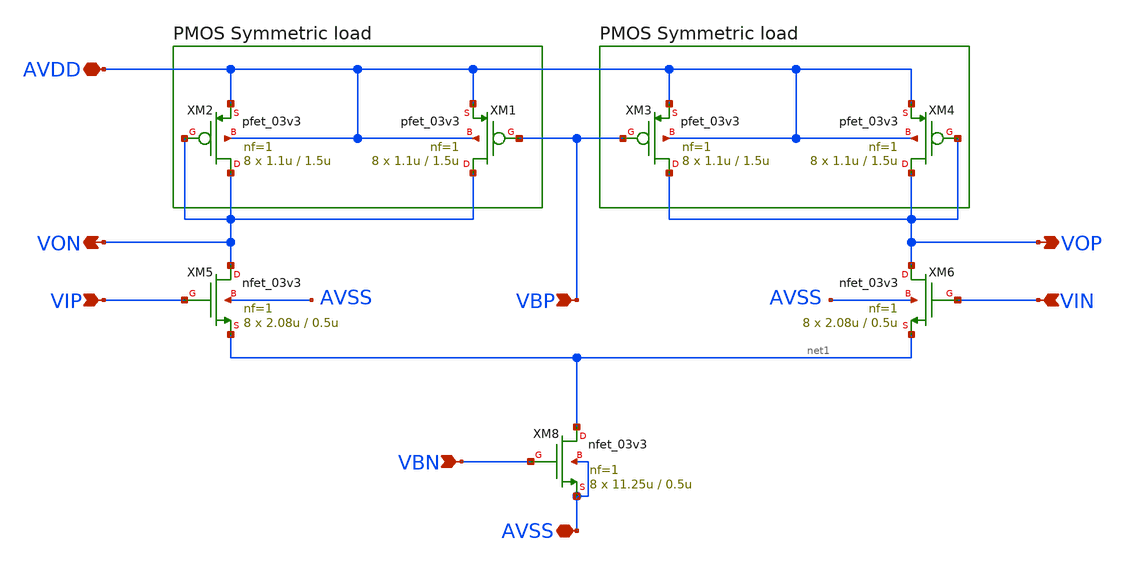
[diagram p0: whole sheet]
** sch_path: designs/libs/core_analog/delay_stage/delay_stage.sch
**.subckt delay_stage VIP VIN VOP VON AVDD AVSS VBP VBN
*.ipin VIP
*.ipin VIN
*.opin VOP
*.opin VON
*.iopin AVDD
*.iopin AVSS
*.ipin VBP
*.ipin VBN
XM5 VON VIP net1 AVSS nfet_03v3 L=0.5u W=2.08u nf=1 ad='int((nf+1)/2) * W/nf * 0.18u' as='int((nf+2)/2) * W/nf * 0.18u'
+ pd='2*int((nf+1)/2) * (W/nf + 0.18u)' ps='2*int((nf+2)/2) * (W/nf + 0.18u)' nrd='0.18u / W' nrs='0.18u / W'
+ sa=0 sb=0 sd=0 m=8
XM2 VON VON AVDD AVDD pfet_03v3 L=1.5u W=1.1u nf=1 ad='int((nf+1)/2) * W/nf * 0.18u' as='int((nf+2)/2) * W/nf * 0.18u'
+ pd='2*int((nf+1)/2) * (W/nf + 0.18u)' ps='2*int((nf+2)/2) * (W/nf + 0.18u)' nrd='0.18u / W' nrs='0.18u / W'
+ sa=0 sb=0 sd=0 m=8
XM6 VOP VIN net1 AVSS nfet_03v3 L=0.5u W=2.08u nf=1 ad='int((nf+1)/2) * W/nf * 0.18u' as='int((nf+2)/2) * W/nf * 0.18u'
+ pd='2*int((nf+1)/2) * (W/nf + 0.18u)' ps='2*int((nf+2)/2) * (W/nf + 0.18u)' nrd='0.18u / W' nrs='0.18u / W'
+ sa=0 sb=0 sd=0 m=8
XM1 VON VBP AVDD AVDD pfet_03v3 L=1.5u W=1.1u nf=1 ad='int((nf+1)/2) * W/nf * 0.18u' as='int((nf+2)/2) * W/nf * 0.18u'
+ pd='2*int((nf+1)/2) * (W/nf + 0.18u)' ps='2*int((nf+2)/2) * (W/nf + 0.18u)' nrd='0.18u / W' nrs='0.18u / W'
+ sa=0 sb=0 sd=0 m=8
XM3 VOP VBP AVDD AVDD pfet_03v3 L=1.5u W=1.1u nf=1 ad='int((nf+1)/2) * W/nf * 0.18u' as='int((nf+2)/2) * W/nf * 0.18u'
+ pd='2*int((nf+1)/2) * (W/nf + 0.18u)' ps='2*int((nf+2)/2) * (W/nf + 0.18u)' nrd='0.18u / W' nrs='0.18u / W'
+ sa=0 sb=0 sd=0 m=8
XM4 VOP VOP AVDD AVDD pfet_03v3 L=1.5u W=1.1u nf=1 ad='int((nf+1)/2) * W/nf * 0.18u' as='int((nf+2)/2) * W/nf * 0.18u'
+ pd='2*int((nf+1)/2) * (W/nf + 0.18u)' ps='2*int((nf+2)/2) * (W/nf + 0.18u)' nrd='0.18u / W' nrs='0.18u / W'
+ sa=0 sb=0 sd=0 m=8
XM8 net1 VBN AVSS AVSS nfet_03v3 L=0.5u W=11.25u nf=1 ad='int((nf+1)/2) * W/nf * 0.18u' as='int((nf+2)/2) * W/nf * 0.18u'
+ pd='2*int((nf+1)/2) * (W/nf + 0.18u)' ps='2*int((nf+2)/2) * (W/nf + 0.18u)' nrd='0.18u / W' nrs='0.18u / W'
+ sa=0 sb=0 sd=0 m=8
**.ends
.end
